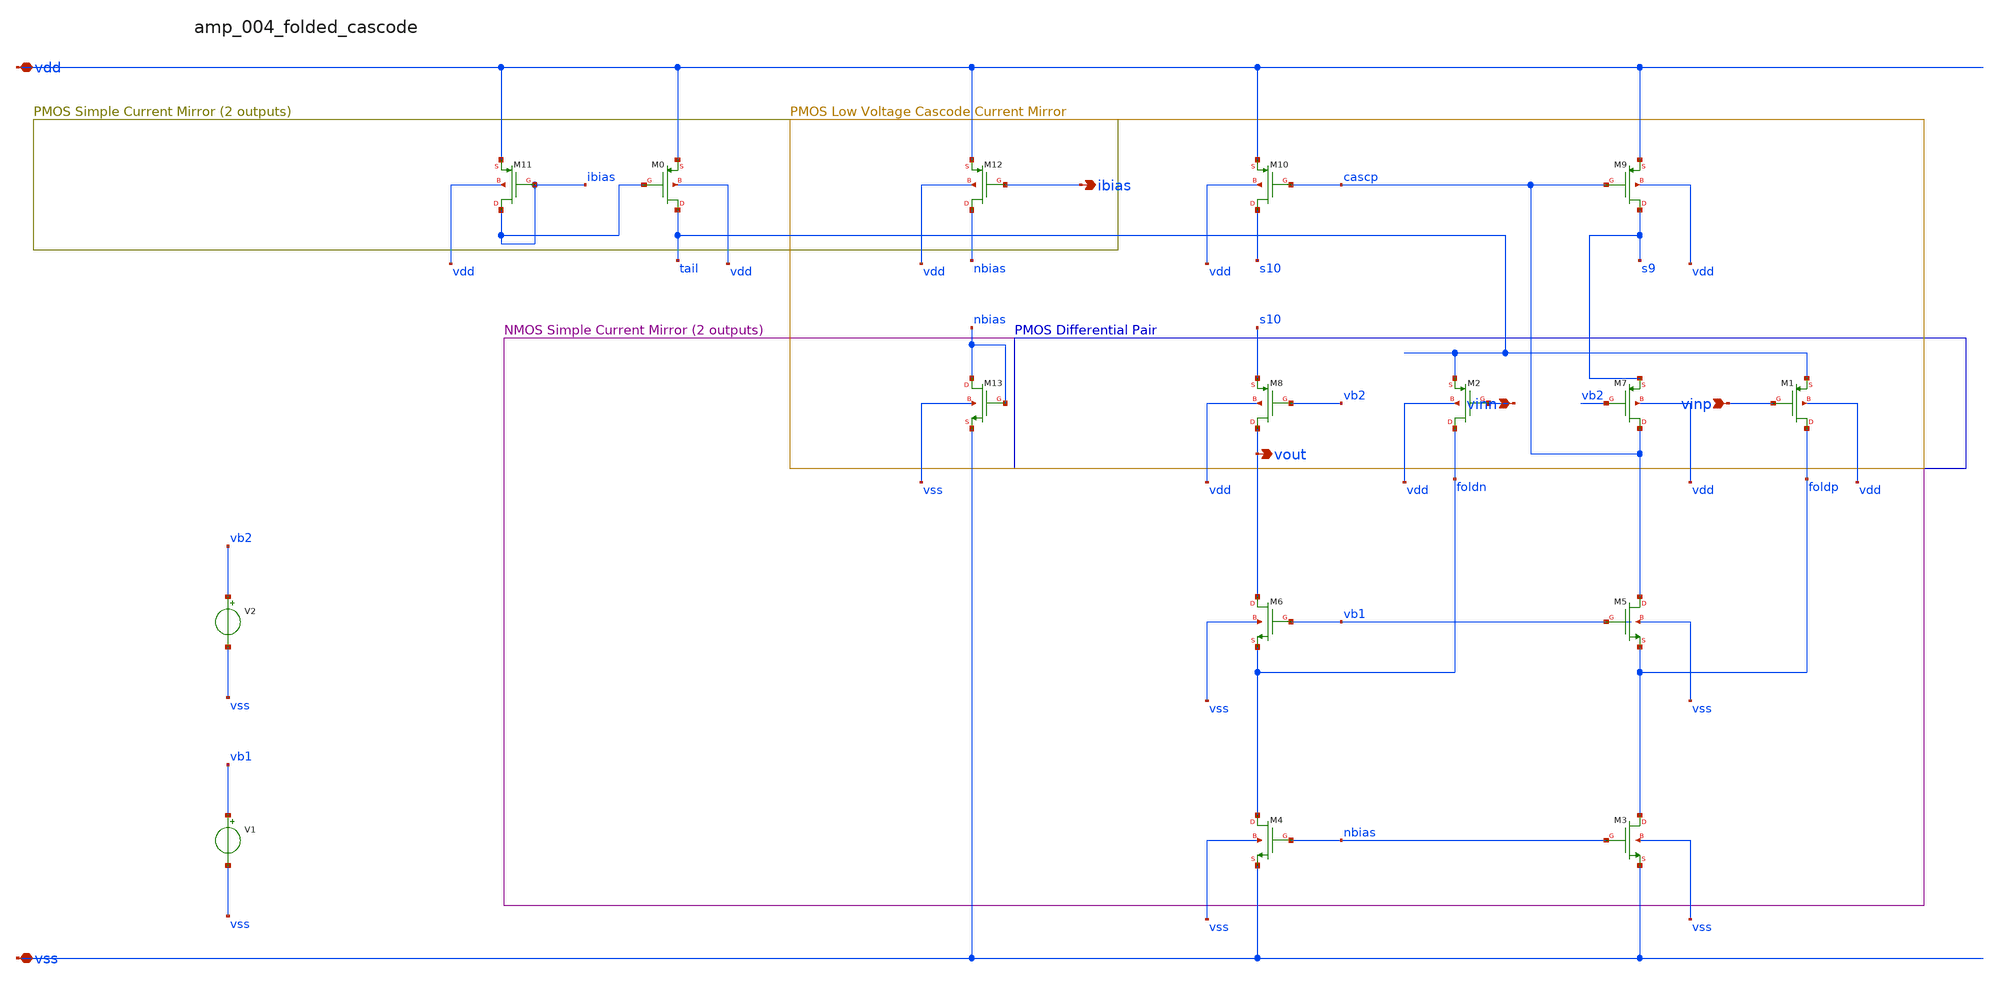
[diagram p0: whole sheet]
** sch_path: analog-db/raw/amp_004_folded_cascode/amp_004_folded_cascode_annotated.sch
**.subckt amp_004_folded_cascode_annotated vinn vinp vdd vss ibias vout
*.ipin vinn
*.ipin vinp
*.iopin vdd
*.iopin vss
*.opin ibias
*.opin vout
V1 vb1 vss x_dut_vb1
V2 vb2 vss x_dut_vb2
XM0 tail ibias vdd vdd sg13_lv_pmos w=x_dut_xm0_w l=x_dut_xm0_l ng=x_dut_xm0_ng m=x_dut_xm0_m
XM1 foldp vinp tail vdd sg13_lv_pmos w=x_dut_xm1_w l=x_dut_xm1_l ng=x_dut_xm1_ng m=x_dut_xm1_m
XM10 s10 cascp vdd vdd sg13_lv_pmos w=x_dut_xm10_w l=x_dut_xm10_l ng=x_dut_xm10_ng m=x_dut_xm10_m
XM11 ibias ibias vdd vdd sg13_lv_pmos w=x_dut_xm11_w l=x_dut_xm11_l ng=x_dut_xm11_ng m=x_dut_xm11_m
XM12 nbias ibias vdd vdd sg13_lv_pmos w=x_dut_xm12_w l=x_dut_xm12_l ng=x_dut_xm12_ng m=x_dut_xm12_m
XM13 nbias nbias vss vss sg13_lv_nmos w=x_dut_xm13_w l=x_dut_xm13_l ng=x_dut_xm13_ng m=x_dut_xm13_m
XM2 foldn vinn tail vdd sg13_lv_pmos w=x_dut_xm2_w l=x_dut_xm2_l ng=x_dut_xm2_ng m=x_dut_xm2_m
XM3 foldp nbias vss vss sg13_lv_nmos w=x_dut_xm3_w l=x_dut_xm3_l ng=x_dut_xm3_ng m=x_dut_xm3_m
XM4 foldn nbias vss vss sg13_lv_nmos w=x_dut_xm4_w l=x_dut_xm4_l ng=x_dut_xm4_ng m=x_dut_xm4_m
XM5 cascp vb1 foldp vss sg13_lv_nmos w=x_dut_xm5_w l=x_dut_xm5_l ng=x_dut_xm5_ng m=x_dut_xm5_m
XM6 vout vb1 foldn vss sg13_lv_nmos w=x_dut_xm6_w l=x_dut_xm6_l ng=x_dut_xm6_ng m=x_dut_xm6_m
XM7 cascp vb2 s9 vdd sg13_lv_pmos w=x_dut_xm7_w l=x_dut_xm7_l ng=x_dut_xm7_ng m=x_dut_xm7_m
XM8 vout vb2 s10 vdd sg13_lv_pmos w=x_dut_xm8_w l=x_dut_xm8_l ng=x_dut_xm8_ng m=x_dut_xm8_m
XM9 s9 cascp vdd vdd sg13_lv_pmos w=x_dut_xm9_w l=x_dut_xm9_l ng=x_dut_xm9_ng m=x_dut_xm9_m
**.ends
.end
